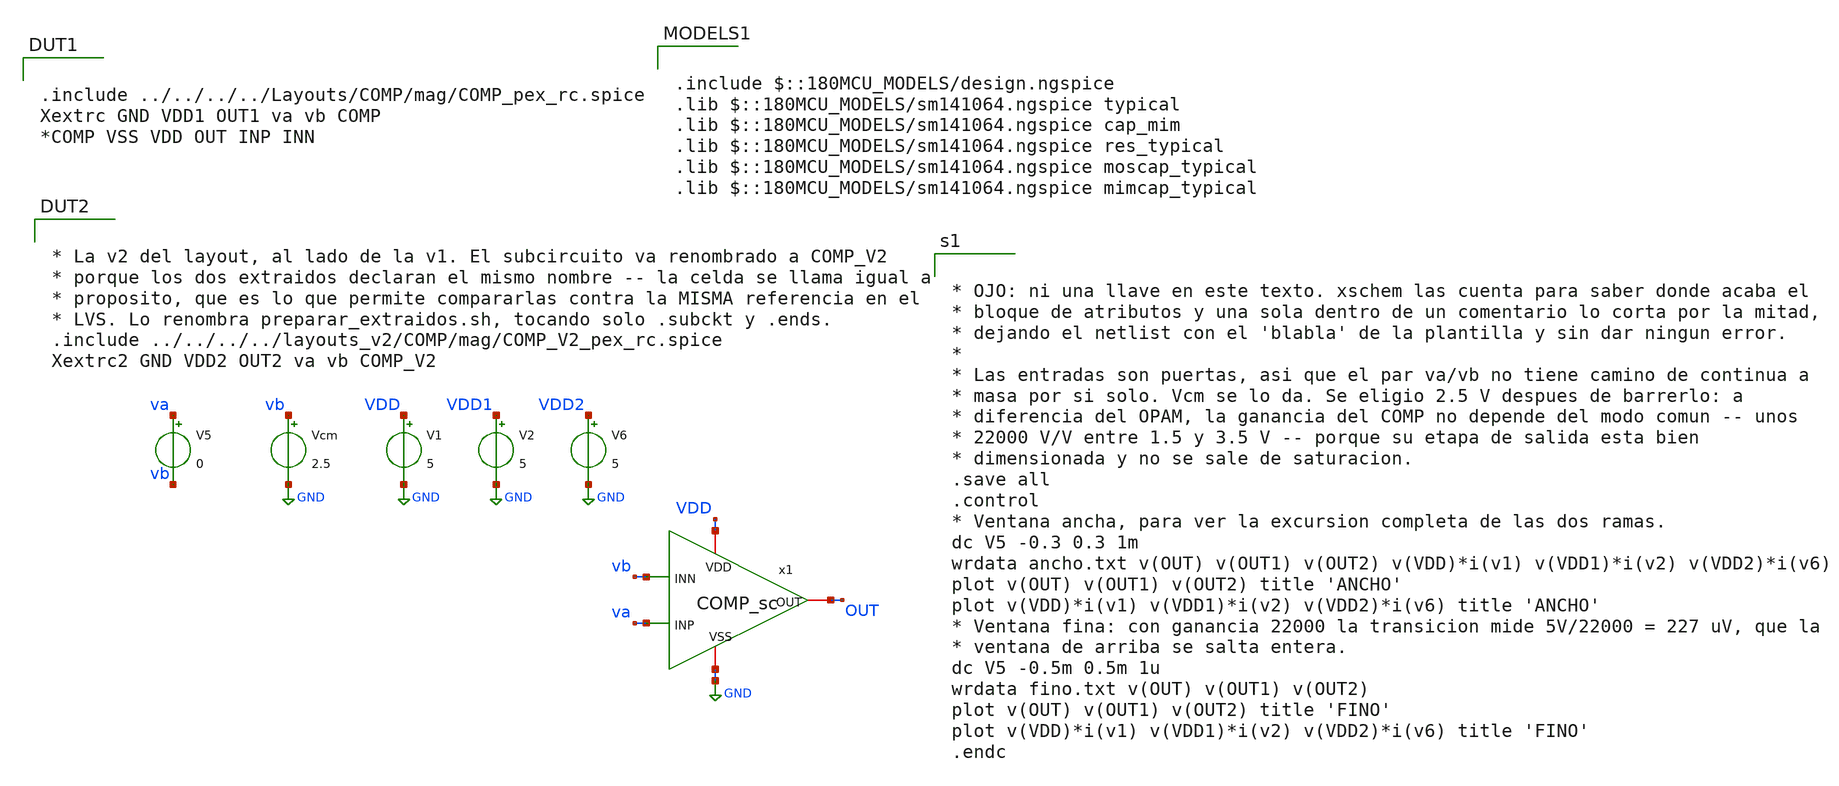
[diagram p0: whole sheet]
** sch_path: FINAL/XSCHEM/TEST_TOTAL/test_TOTAL.sch
**.subckt test_TOTAL
V1 VDD GND 5
V2 VDD1 GND 5
V6 VDD2 GND 5
V5 va vb 0
Vcm vb GND 2.5
x1 VDD vb OUT va GND COMP_sc
**** begin user architecture code

.include $::180MCU_MODELS/design.ngspice
.lib $::180MCU_MODELS/sm141064.ngspice typical
.lib $::180MCU_MODELS/sm141064.ngspice cap_mim
.lib $::180MCU_MODELS/sm141064.ngspice res_typical
.lib $::180MCU_MODELS/sm141064.ngspice moscap_typical
.lib $::180MCU_MODELS/sm141064.ngspice mimcap_typical


.include ../../../../Layouts/COMP/mag/COMP_pex_rc.spice
Xextrc GND VDD1 OUT1 va vb COMP
*COMP VSS VDD OUT INP INN


* La v2 del layout, al lado de la v1. El subcircuito va renombrado a COMP_V2
* porque los dos extraidos declaran el mismo nombre -- la celda se llama igual a
* proposito, que es lo que permite compararlas contra la MISMA referencia en el
* LVS. Lo renombra preparar_extraidos.sh, tocando solo .subckt y .ends.
.include ../../../../layouts_v2/COMP/mag/COMP_V2_pex_rc.spice
Xextrc2 GND VDD2 OUT2 va vb COMP_V2



* OJO: ni una llave en este texto. xschem las cuenta para saber donde acaba el
* bloque de atributos y una sola dentro de un comentario lo corta por la mitad,
* dejando el netlist con el 'blabla' de la plantilla y sin dar ningun error.
*
* Las entradas son puertas, asi que el par va/vb no tiene camino de continua a
* masa por si solo. Vcm se lo da. Se eligio 2.5 V despues de barrerlo: a
* diferencia del OPAM, la ganancia del COMP no depende del modo comun -- unos
* 22000 V/V entre 1.5 y 3.5 V -- porque su etapa de salida esta bien
* dimensionada y no se sale de saturacion.
.save all
.control
* Ventana ancha, para ver la excursion completa de las dos ramas.
dc V5 -0.3 0.3 1m
wrdata ancho.txt v(OUT) v(OUT1) v(OUT2) v(VDD)*i(v1) v(VDD1)*i(v2) v(VDD2)*i(v6)
plot v(OUT) v(OUT1) v(OUT2) title 'ANCHO'
plot v(VDD)*i(v1) v(VDD1)*i(v2) v(VDD2)*i(v6) title 'ANCHO'
* Ventana fina: con ganancia 22000 la transicion mide 5V/22000 = 227 uV, que la
* ventana de arriba se salta entera.
dc V5 -0.5m 0.5m 1u
wrdata fino.txt v(OUT) v(OUT1) v(OUT2)
plot v(OUT) v(OUT1) v(OUT2) title 'FINO'
plot v(VDD)*i(v1) v(VDD1)*i(v2) v(VDD2)*i(v6) title 'FINO'
.endc


**** end user architecture code
**.ends
.GLOBAL GND
.end
